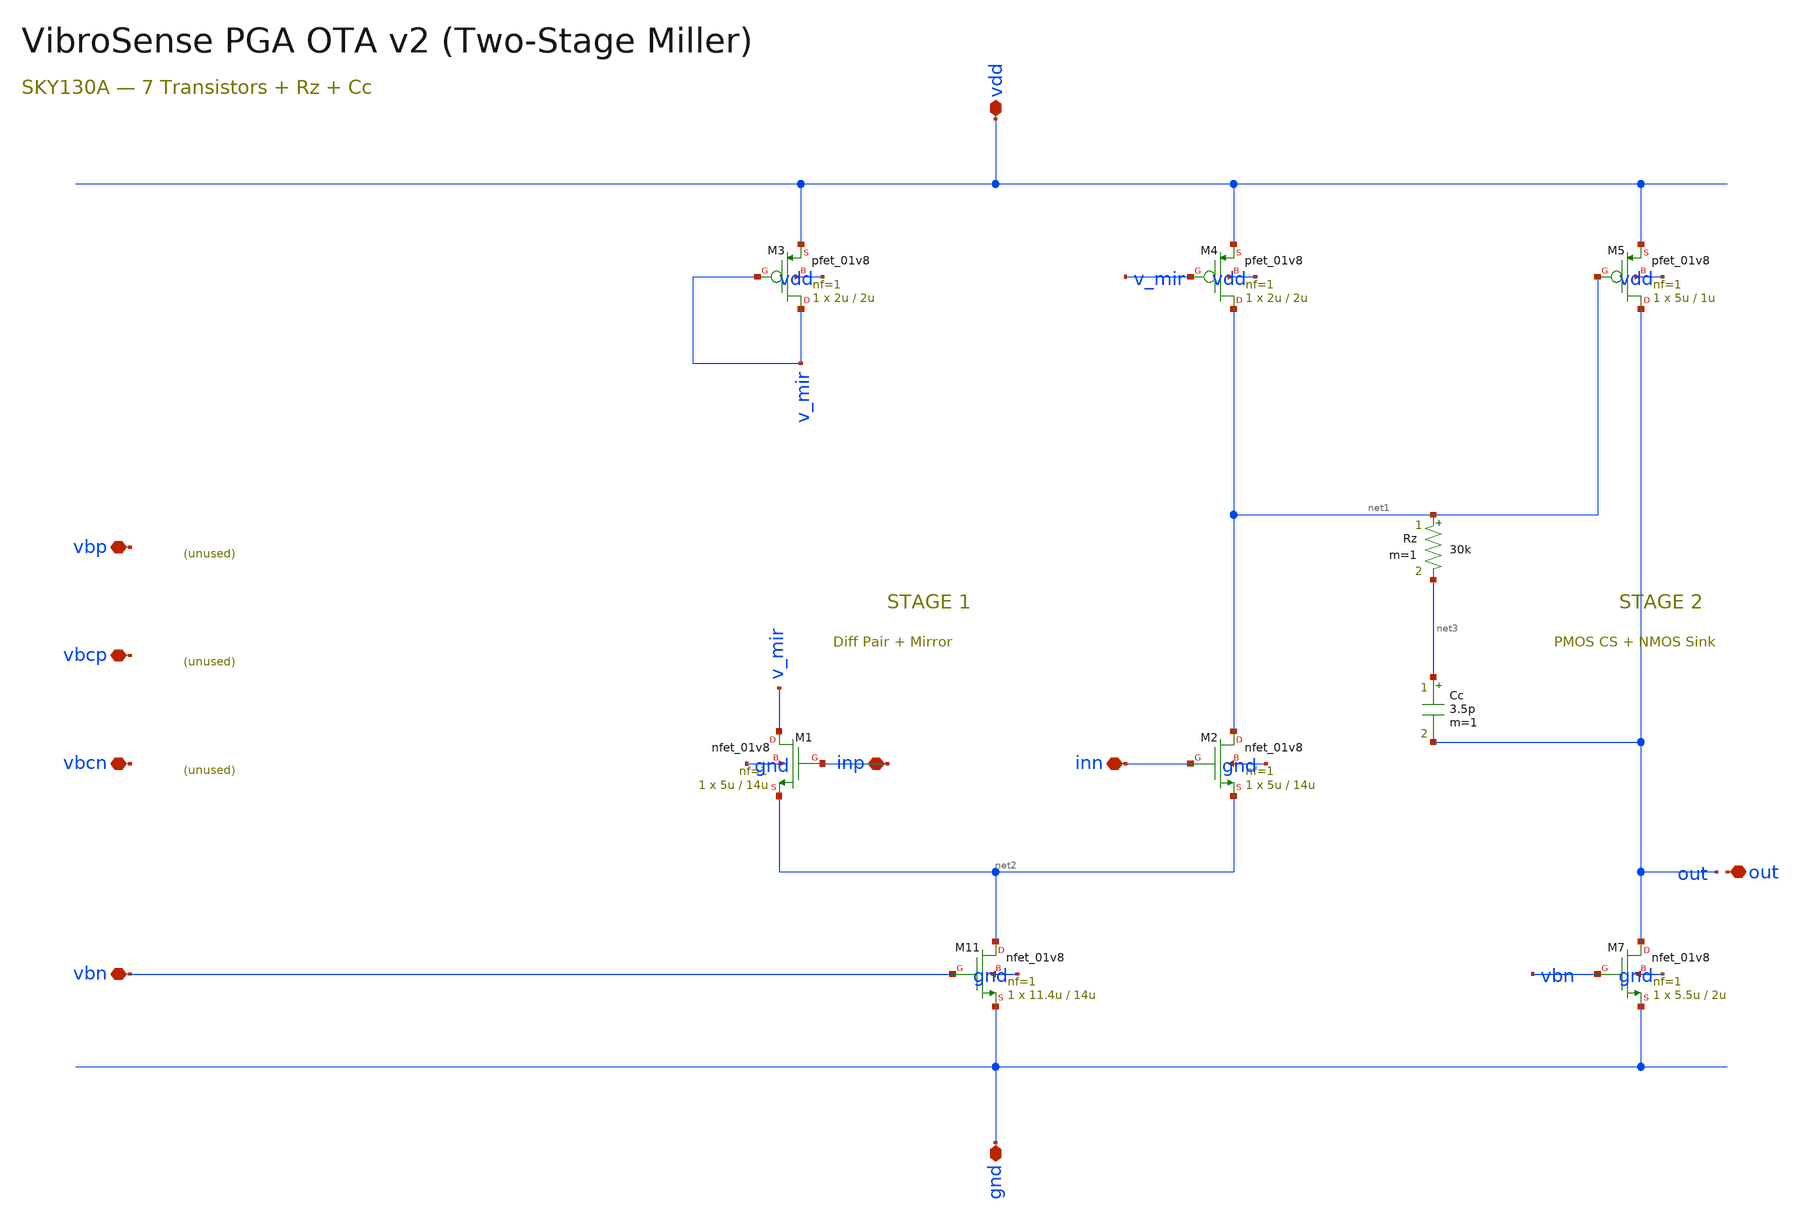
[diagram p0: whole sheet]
** sch_path: vibrosense/01_ota/ota_pga_v2/schematic/ota_pga_v2.sch
**.subckt ota_pga_v2 inp inn out vdd gnd vbn vbp vbcp vbcn
*.iopin inp
*.iopin inn
*.iopin out
*.iopin vdd
*.iopin gnd
*.iopin vbn
*.iopin vbp
*.iopin vbcp
*.iopin vbcn
XM3 v_mir v_mir vdd vdd sky130_fd_pr__pfet_01v8 L=2u W=2u nf=1 ad='int((nf+1)/2) * W/nf * 0.29' as='int((nf+2)/2) * W/nf * 0.29'
+ pd='2*int((nf+1)/2) * (W/nf + 0.29)' ps='2*int((nf+2)/2) * (W/nf + 0.29)' nrd='0.29 / W' nrs='0.29 / W'
+ sa=0 sb=0 sd=0 mult=1 m=1
XM4 net1 v_mir vdd vdd sky130_fd_pr__pfet_01v8 L=2u W=2u nf=1 ad='int((nf+1)/2) * W/nf * 0.29' as='int((nf+2)/2) * W/nf * 0.29'
+ pd='2*int((nf+1)/2) * (W/nf + 0.29)' ps='2*int((nf+2)/2) * (W/nf + 0.29)' nrd='0.29 / W' nrs='0.29 / W'
+ sa=0 sb=0 sd=0 mult=1 m=1
XM5 out net1 vdd vdd sky130_fd_pr__pfet_01v8 L=1u W=5u nf=1 ad='int((nf+1)/2) * W/nf * 0.29' as='int((nf+2)/2) * W/nf * 0.29'
+ pd='2*int((nf+1)/2) * (W/nf + 0.29)' ps='2*int((nf+2)/2) * (W/nf + 0.29)' nrd='0.29 / W' nrs='0.29 / W'
+ sa=0 sb=0 sd=0 mult=1 m=1
XM1 v_mir inp net2 gnd sky130_fd_pr__nfet_01v8 L=14u W=5u nf=1 ad='int((1 + 1)/2) * 5u / 1 * 0.29' as='int((1 + 2)/2) * 5u / 1 * 0.29'
+ pd='2*int((1 + 1)/2) * (5u / 1 + 0.29)' ps='2*int((1 + 2)/2) * (5u / 1 + 0.29)' nrd='0.29 / 5u ' nrs='0.29 / 5u '
+ sa=0 sb=0 sd=0 mult=1 m=1
XM2 net1 inn net2 gnd sky130_fd_pr__nfet_01v8 L=14u W=5u nf=1 ad='int((1 + 1)/2) * 5u / 1 * 0.29' as='int((1 + 2)/2) * 5u / 1 * 0.29'
+ pd='2*int((1 + 1)/2) * (5u / 1 + 0.29)' ps='2*int((1 + 2)/2) * (5u / 1 + 0.29)' nrd='0.29 / 5u ' nrs='0.29 / 5u '
+ sa=0 sb=0 sd=0 mult=1 m=1
XM11 net2 vbn gnd gnd sky130_fd_pr__nfet_01v8 L=14u W=11.4u nf=1 ad='int((1 + 1)/2) * 11.4u / 1 * 0.29'
+ as='int((1 + 2)/2) * 11.4u / 1 * 0.29' pd='2*int((1 + 1)/2) * (11.4u / 1 + 0.29)' ps='2*int((1 + 2)/2) * (11.4u / 1 + 0.29)'
+ nrd='0.29 / 11.4u ' nrs='0.29 / 11.4u ' sa=0 sb=0 sd=0 mult=1 m=1
XM7 out vbn gnd gnd sky130_fd_pr__nfet_01v8 L=2u W=5.5u nf=1 ad='int((1 + 1)/2) * 5.5u / 1 * 0.29' as='int((1 + 2)/2) * 5.5u / 1 * 0.29'
+ pd='2*int((1 + 1)/2) * (5.5u / 1 + 0.29)' ps='2*int((1 + 2)/2) * (5.5u / 1 + 0.29)' nrd='0.29 / 5.5u '
+ nrs='0.29 / 5.5u ' sa=0 sb=0 sd=0 mult=1 m=1
Rz net1 net3 30k m=1
Cc net3 out 3.5p m=1
**.ends
.end
